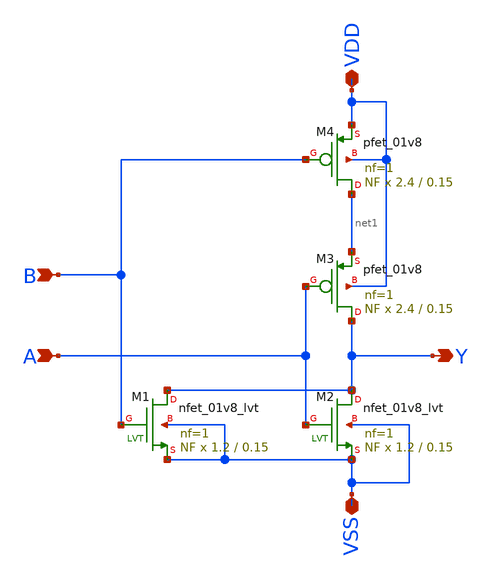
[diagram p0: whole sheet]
** sch_path: xschem_lib/DFFRAM_full_custom/nor.sch
**.subckt nor VDD VSS Y A B
*.iopin VDD
*.iopin VSS
*.opin Y
*.ipin A
*.ipin B
XM1 Y B VSS VSS sky130_fd_pr__nfet_01v8_lvt L=0.15 W=1.2 nf=1 ad='int((nf+1)/2) * W/nf * 0.29' as='int((nf+2)/2) * W/nf * 0.29'
+ pd='2*int((nf+1)/2) * (W/nf + 0.29)' ps='2*int((nf+2)/2) * (W/nf + 0.29)' nrd='0.29 / W' nrs='0.29 / W'
+ sa=0 sb=0 sd=0 mult=NF m=NF
XM2 Y A VSS VSS sky130_fd_pr__nfet_01v8_lvt L=0.15 W=1.2 nf=1 ad='int((nf+1)/2) * W/nf * 0.29' as='int((nf+2)/2) * W/nf * 0.29'
+ pd='2*int((nf+1)/2) * (W/nf + 0.29)' ps='2*int((nf+2)/2) * (W/nf + 0.29)' nrd='0.29 / W' nrs='0.29 / W'
+ sa=0 sb=0 sd=0 mult=NF m=NF
XM3 Y A net1 VDD sky130_fd_pr__pfet_01v8 L=0.15 W=2.4 nf=1 ad='int((nf+1)/2) * W/nf * 0.29' as='int((nf+2)/2) * W/nf * 0.29'
+ pd='2*int((nf+1)/2) * (W/nf + 0.29)' ps='2*int((nf+2)/2) * (W/nf + 0.29)' nrd='0.29 / W' nrs='0.29 / W'
+ sa=0 sb=0 sd=0 mult=NF m=NF
XM4 net1 B VDD VDD sky130_fd_pr__pfet_01v8 L=0.15 W=2.4 nf=1 ad='int((nf+1)/2) * W/nf * 0.29' as='int((nf+2)/2) * W/nf * 0.29'
+ pd='2*int((nf+1)/2) * (W/nf + 0.29)' ps='2*int((nf+2)/2) * (W/nf + 0.29)' nrd='0.29 / W' nrs='0.29 / W'
+ sa=0 sb=0 sd=0 mult=NF m=NF
**.ends
.end
